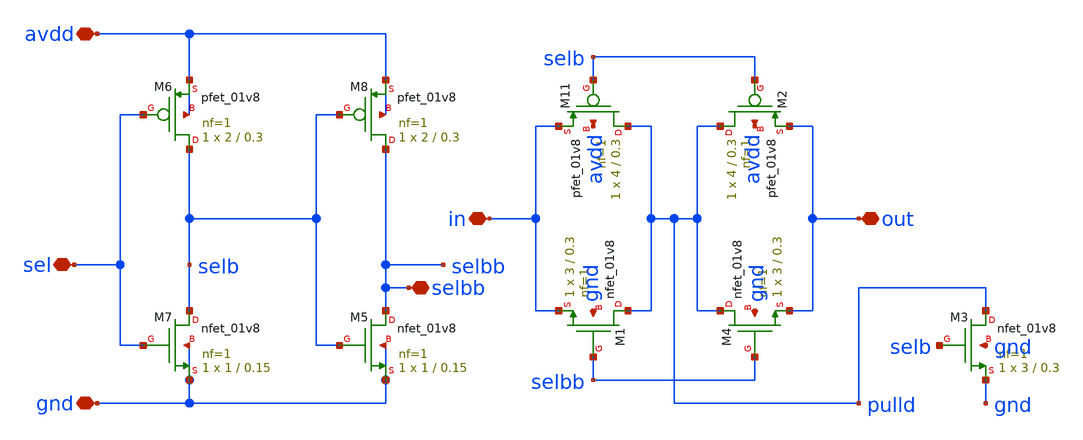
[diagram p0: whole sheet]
** sch_path: xschem/rev_1/amux.sch
**.subckt amux avdd gnd in out sel selbb
*.iopin avdd
*.iopin gnd
*.iopin in
*.iopin out
*.iopin sel
*.iopin selbb
XM11 pulld selb in avdd sky130_fd_pr__pfet_01v8 L=0.3 W=4 nf=1 ad='int((nf+1)/2) * W/nf * 0.29' as='int((nf+2)/2) * W/nf * 0.29'
+ pd='2*int((nf+1)/2) * (W/nf + 0.29)' ps='2*int((nf+2)/2) * (W/nf + 0.29)' nrd='0.29 / W' nrs='0.29 / W'
+ sa=0 sb=0 sd=0 mult=1 m=1
XM1 pulld selbb in gnd sky130_fd_pr__nfet_01v8 L=0.3 W=3 nf=1 ad='int((1 + 1)/2) * 3 / 1 * 0.29' as='int((1 + 2)/2) * 3 / 1 * 0.29'
+ pd='2*int((1 + 1)/2) * (3 / 1 + 0.29)' ps='2*int((1 + 2)/2) * (3 / 1 + 0.29)' nrd='0.29 / 3 ' nrs='0.29 / 3 '
+ sa=0 sb=0 sd=0 mult=1 m=1
XM3 pulld selb gnd gnd sky130_fd_pr__nfet_01v8 L=0.3 W=3 nf=1 ad='int((1 + 1)/2) * 3 / 1 * 0.29' as='int((1 + 2)/2) * 3 / 1 * 0.29'
+ pd='2*int((1 + 1)/2) * (3 / 1 + 0.29)' ps='2*int((1 + 2)/2) * (3 / 1 + 0.29)' nrd='0.29 / 3 ' nrs='0.29 / 3 '
+ sa=0 sb=0 sd=0 mult=1 m=1
XM5 selbb selb gnd gnd sky130_fd_pr__nfet_01v8 L=0.15 W=1 nf=1 ad='int((1 + 1)/2) * 1 / 1 * 0.29' as='int((1 + 2)/2) * 1 / 1 * 0.29'
+ pd='2*int((1 + 1)/2) * (1 / 1 + 0.29)' ps='2*int((1 + 2)/2) * (1 / 1 + 0.29)' nrd='0.29 / 1 ' nrs='0.29 / 1 '
+ sa=0 sb=0 sd=0 mult=1 m=1
XM6 selb sel avdd avdd sky130_fd_pr__pfet_01v8 L=0.3 W=2 nf=1 ad='int((nf+1)/2) * W/nf * 0.29' as='int((nf+2)/2) * W/nf * 0.29'
+ pd='2*int((nf+1)/2) * (W/nf + 0.29)' ps='2*int((nf+2)/2) * (W/nf + 0.29)' nrd='0.29 / W' nrs='0.29 / W'
+ sa=0 sb=0 sd=0 mult=1 m=1
XM7 selb sel gnd gnd sky130_fd_pr__nfet_01v8 L=0.15 W=1 nf=1 ad='int((1 + 1)/2) * 1 / 1 * 0.29' as='int((1 + 2)/2) * 1 / 1 * 0.29'
+ pd='2*int((1 + 1)/2) * (1 / 1 + 0.29)' ps='2*int((1 + 2)/2) * (1 / 1 + 0.29)' nrd='0.29 / 1 ' nrs='0.29 / 1 '
+ sa=0 sb=0 sd=0 mult=1 m=1
XM8 selbb selb avdd avdd sky130_fd_pr__pfet_01v8 L=0.3 W=2 nf=1 ad='int((nf+1)/2) * W/nf * 0.29' as='int((nf+2)/2) * W/nf * 0.29'
+ pd='2*int((nf+1)/2) * (W/nf + 0.29)' ps='2*int((nf+2)/2) * (W/nf + 0.29)' nrd='0.29 / W' nrs='0.29 / W'
+ sa=0 sb=0 sd=0 mult=1 m=1
XM2 pulld selb out avdd sky130_fd_pr__pfet_01v8 L=0.3 W=4 nf=1 ad='int((nf+1)/2) * W/nf * 0.29' as='int((nf+2)/2) * W/nf * 0.29'
+ pd='2*int((nf+1)/2) * (W/nf + 0.29)' ps='2*int((nf+2)/2) * (W/nf + 0.29)' nrd='0.29 / W' nrs='0.29 / W'
+ sa=0 sb=0 sd=0 mult=1 m=1
XM4 pulld selbb out gnd sky130_fd_pr__nfet_01v8 L=0.3 W=3 nf=1 ad='int((1 + 1)/2) * 3 / 1 * 0.29' as='int((1 + 2)/2) * 3 / 1 * 0.29'
+ pd='2*int((1 + 1)/2) * (3 / 1 + 0.29)' ps='2*int((1 + 2)/2) * (3 / 1 + 0.29)' nrd='0.29 / 3 ' nrs='0.29 / 3 '
+ sa=0 sb=0 sd=0 mult=1 m=1
**.ends
.end
